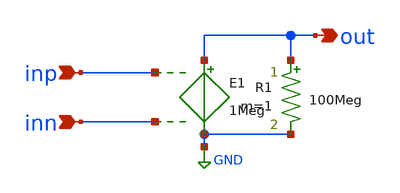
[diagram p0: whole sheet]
** sch_path: 2_ideal_circuits/ideal_opamp.sch
**.subckt ideal_opamp out inp inn
*.opin out
*.ipin inp
*.ipin inn
E1 out GND inp inn 1Meg
R1 out GND 100Meg m=1
**.ends
.GLOBAL GND
.end
